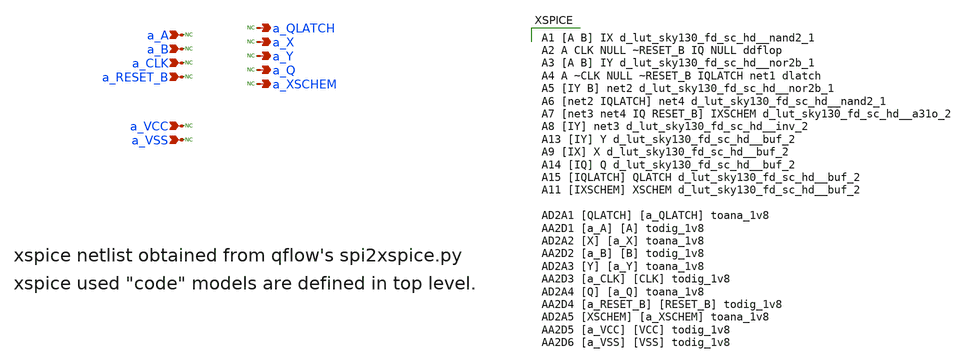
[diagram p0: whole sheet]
** sch_path: sky130_tests/stdcells_xspice.sch
* Copyright 2021 Stefan Frederik Schippers
* Licensed under the Apache License, Version 2.0 (the "License");
* you may not use this file except in compliance with the License.
* You may obtain a copy of the License at
* https://www.apache.org/licenses/LICENSE-2.0
* Unless required by applicable law or agreed to in writing, software
* distributed under the License is distributed on an "AS IS" BASIS,
* WITHOUT WARRANTIES OR CONDITIONS OF ANY KIND, either express or implied.
* See the License for the specific language governing permissions and
* limitations under the License.
**.subckt stdcells_xspice a_RESET_B a_CLK a_B a_A a_Y a_X a_QLATCH a_Q a_XSCHEM a_VCC a_VSS
*.ipin a_RESET_B
*.ipin a_CLK
*.ipin a_B
*.ipin a_A
*.opin a_Y
*.opin a_X
*.opin a_QLATCH
*.opin a_Q
*.opin a_XSCHEM
*.ipin a_VCC
*.ipin a_VSS
* noconn a_A
* noconn a_B
* noconn a_CLK
* noconn a_RESET_B
* noconn a_VCC
* noconn a_VSS
* noconn a_QLATCH
* noconn a_X
* noconn a_Y
* noconn a_Q
* noconn a_XSCHEM
**** begin user architecture code

A1 [A B] IX d_lut_sky130_fd_sc_hd__nand2_1
A2 A CLK NULL ~RESET_B IQ NULL ddflop
A3 [A B] IY d_lut_sky130_fd_sc_hd__nor2b_1
A4 A ~CLK NULL ~RESET_B IQLATCH net1 dlatch
A5 [IY B] net2 d_lut_sky130_fd_sc_hd__nor2b_1
A6 [net2 IQLATCH] net4 d_lut_sky130_fd_sc_hd__nand2_1
A7 [net3 net4 IQ RESET_B] IXSCHEM d_lut_sky130_fd_sc_hd__a31o_2
A8 [IY] net3 d_lut_sky130_fd_sc_hd__inv_2
A13 [IY] Y d_lut_sky130_fd_sc_hd__buf_2
A9 [IX] X d_lut_sky130_fd_sc_hd__buf_2
A14 [IQ] Q d_lut_sky130_fd_sc_hd__buf_2
A15 [IQLATCH] QLATCH d_lut_sky130_fd_sc_hd__buf_2
A11 [IXSCHEM] XSCHEM d_lut_sky130_fd_sc_hd__buf_2

AD2A1 [QLATCH] [a_QLATCH] toana_1v8
AA2D1 [a_A] [A] todig_1v8
AD2A2 [X] [a_X] toana_1v8
AA2D2 [a_B] [B] todig_1v8
AD2A3 [Y] [a_Y] toana_1v8
AA2D3 [a_CLK] [CLK] todig_1v8
AD2A4 [Q] [a_Q] toana_1v8
AA2D4 [a_RESET_B] [RESET_B] todig_1v8
AD2A5 [XSCHEM] [a_XSCHEM] toana_1v8
AA2D5 [a_VCC] [VCC] todig_1v8
AA2D6 [a_VSS] [VSS] todig_1v8


**** end user architecture code
**.ends
.end
